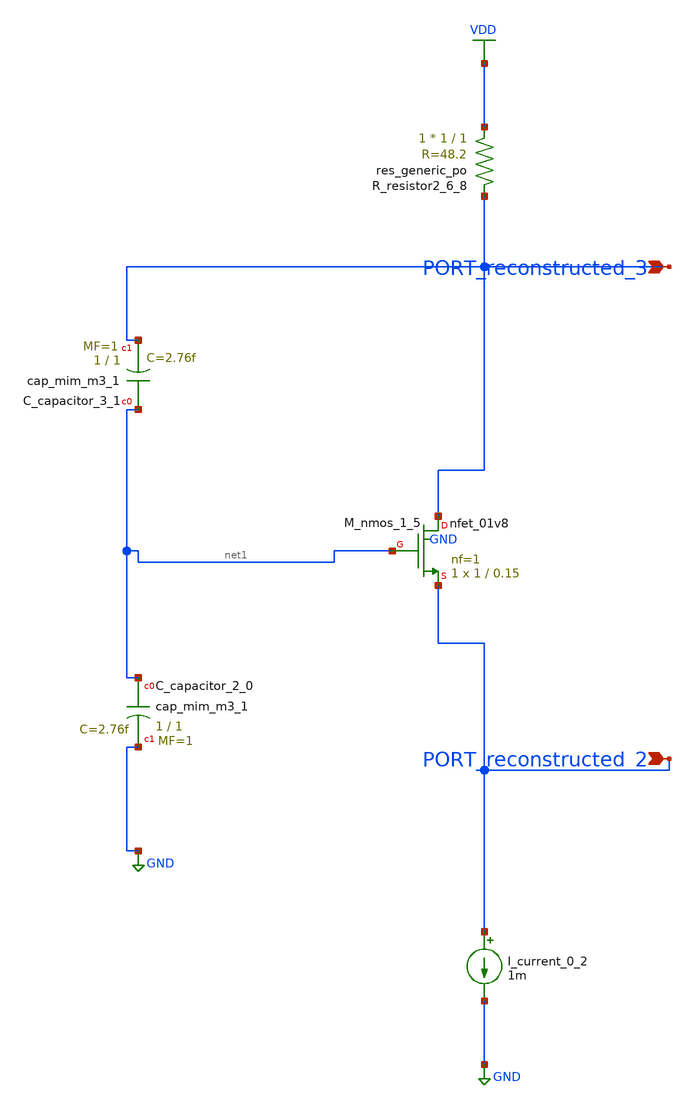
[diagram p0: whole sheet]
** sch_path: schematics/AMSNet/555.sch
**.subckt 555 PORT_reconstructed_2 PORT_reconstructed_3
*.ipin PORT_reconstructed_2
*.ipin PORT_reconstructed_3
XC_capacitor_2_0 net1 GND sky130_fd_pr__cap_mim_m3_1 W=1 L=1 MF=1 m=1
XC_capacitor_3_1 net1 PORT_reconstructed_3 sky130_fd_pr__cap_mim_m3_1 W=1 L=1 MF=1 m=1
I_current_0_2 PORT_reconstructed_2 GND 1m
XM_nmos_1_5 PORT_reconstructed_3 net1 PORT_reconstructed_2 GND sky130_fd_pr__nfet_01v8 L=0.15 W=1 nf=1
+ ad='int((1 + 1)/2) * 1 / 1 * 0.29' as='int((1 + 2)/2) * 1 / 1 * 0.29' pd='2*int((1 + 1)/2) * (1 / 1 + 0.29)'
+ ps='2*int((1 + 2)/2) * (1 / 1 + 0.29)' nrd='0.29 / 1 ' nrs='0.29 / 1 ' sa=0 sb=0 sd=0 mult=1 m=1
XR_resistor2_6_8 VDD PORT_reconstructed_3 sky130_fd_pr__res_generic_po W=1 L=1 m=1
**.ends
.GLOBAL GND
.GLOBAL VDD
.end
